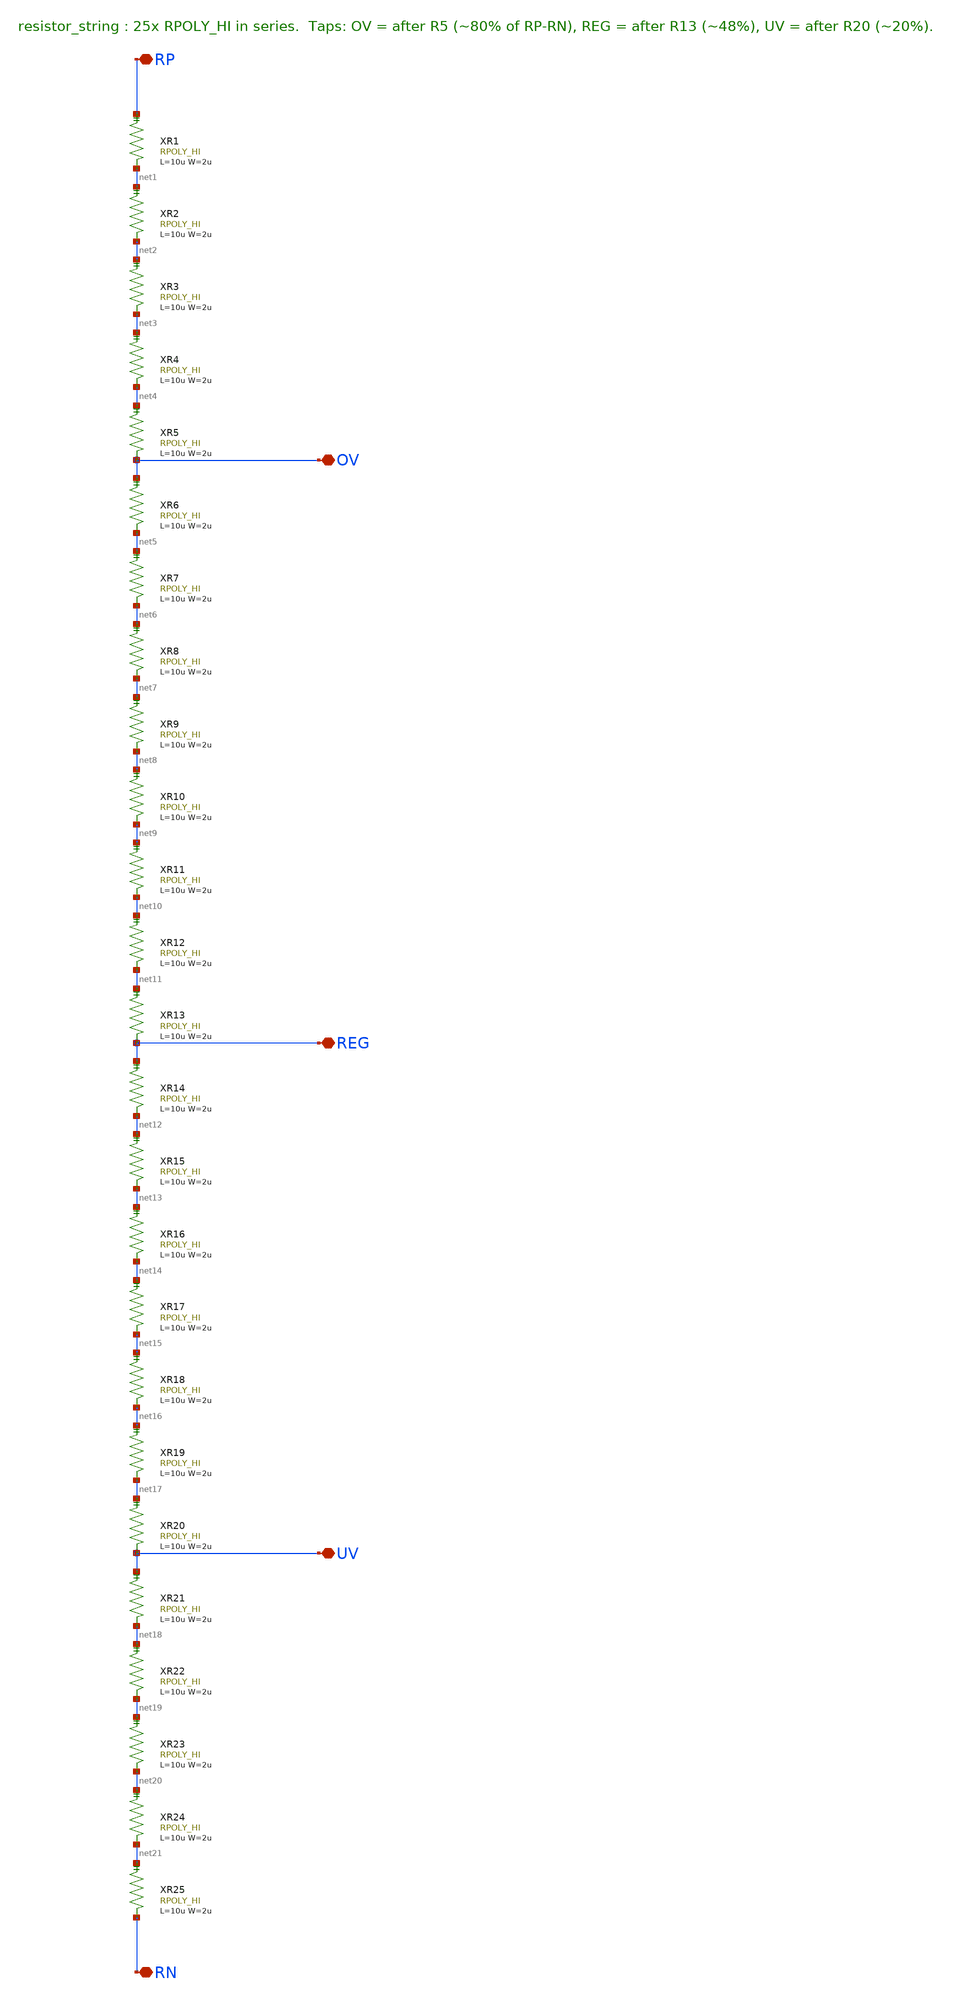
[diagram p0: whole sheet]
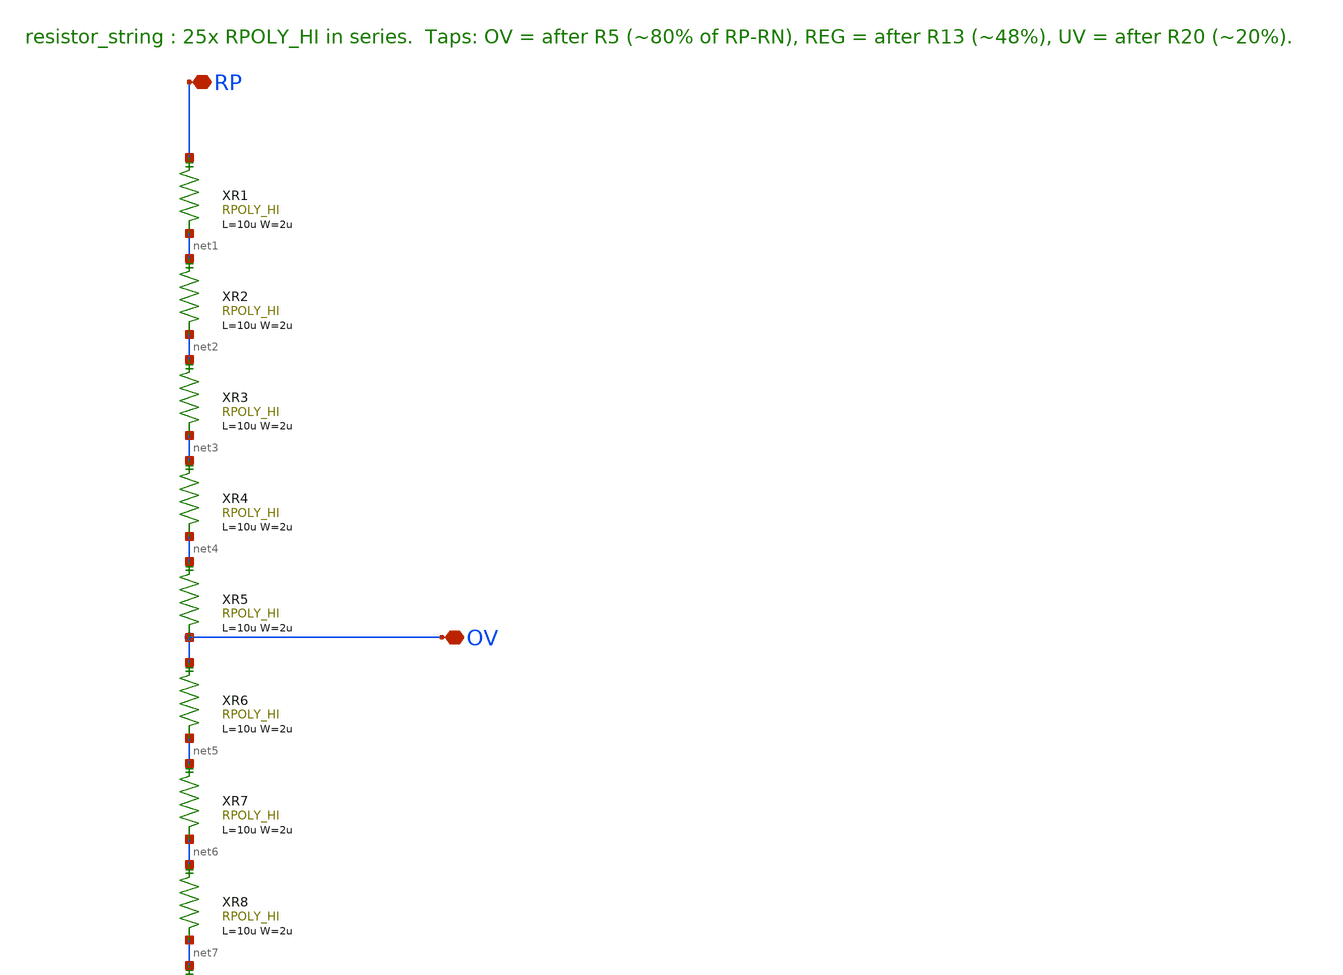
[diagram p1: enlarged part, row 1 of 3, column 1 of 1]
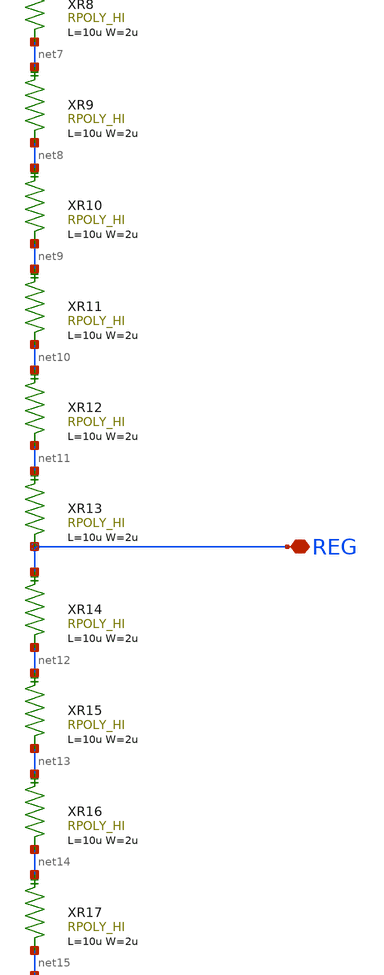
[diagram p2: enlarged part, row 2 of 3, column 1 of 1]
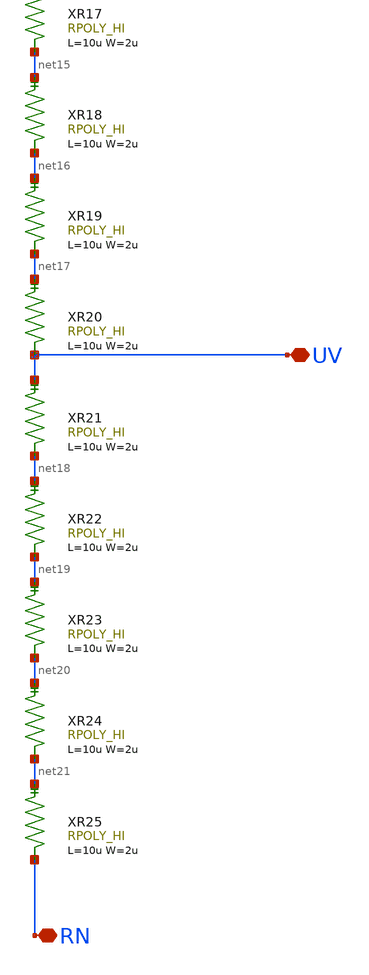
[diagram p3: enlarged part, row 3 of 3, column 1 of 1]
** sch_path: xschem/designs/resistor_string.sch
**.subckt resistor_string RP RN OV REG UV
*.iopin RP
*.iopin RN
*.iopin OV
*.iopin REG
*.iopin UV
XR1 RP net1 RPOLY_HI L=10u W=2u NS=1 M=1 Z_R=0
XR2 net1 net2 RPOLY_HI L=10u W=2u NS=1 M=1 Z_R=0
XR3 net2 net3 RPOLY_HI L=10u W=2u NS=1 M=1 Z_R=0
XR4 net3 net4 RPOLY_HI L=10u W=2u NS=1 M=1 Z_R=0
XR5 net4 OV RPOLY_HI L=10u W=2u NS=1 M=1 Z_R=0
XR6 OV net5 RPOLY_HI L=10u W=2u NS=1 M=1 Z_R=0
XR7 net5 net6 RPOLY_HI L=10u W=2u NS=1 M=1 Z_R=0
XR8 net6 net7 RPOLY_HI L=10u W=2u NS=1 M=1 Z_R=0
XR9 net7 net8 RPOLY_HI L=10u W=2u NS=1 M=1 Z_R=0
XR10 net8 net9 RPOLY_HI L=10u W=2u NS=1 M=1 Z_R=0
XR11 net9 net10 RPOLY_HI L=10u W=2u NS=1 M=1 Z_R=0
XR12 net10 net11 RPOLY_HI L=10u W=2u NS=1 M=1 Z_R=0
XR13 net11 REG RPOLY_HI L=10u W=2u NS=1 M=1 Z_R=0
XR14 REG net12 RPOLY_HI L=10u W=2u NS=1 M=1 Z_R=0
XR15 net12 net13 RPOLY_HI L=10u W=2u NS=1 M=1 Z_R=0
XR16 net13 net14 RPOLY_HI L=10u W=2u NS=1 M=1 Z_R=0
XR17 net14 net15 RPOLY_HI L=10u W=2u NS=1 M=1 Z_R=0
XR18 net15 net16 RPOLY_HI L=10u W=2u NS=1 M=1 Z_R=0
XR19 net16 net17 RPOLY_HI L=10u W=2u NS=1 M=1 Z_R=0
XR20 net17 UV RPOLY_HI L=10u W=2u NS=1 M=1 Z_R=0
XR21 UV net18 RPOLY_HI L=10u W=2u NS=1 M=1 Z_R=0
XR22 net18 net19 RPOLY_HI L=10u W=2u NS=1 M=1 Z_R=0
XR23 net19 net20 RPOLY_HI L=10u W=2u NS=1 M=1 Z_R=0
XR24 net20 net21 RPOLY_HI L=10u W=2u NS=1 M=1 Z_R=0
XR25 net21 RN RPOLY_HI L=10u W=2u NS=1 M=1 Z_R=0
**.ends
.end
